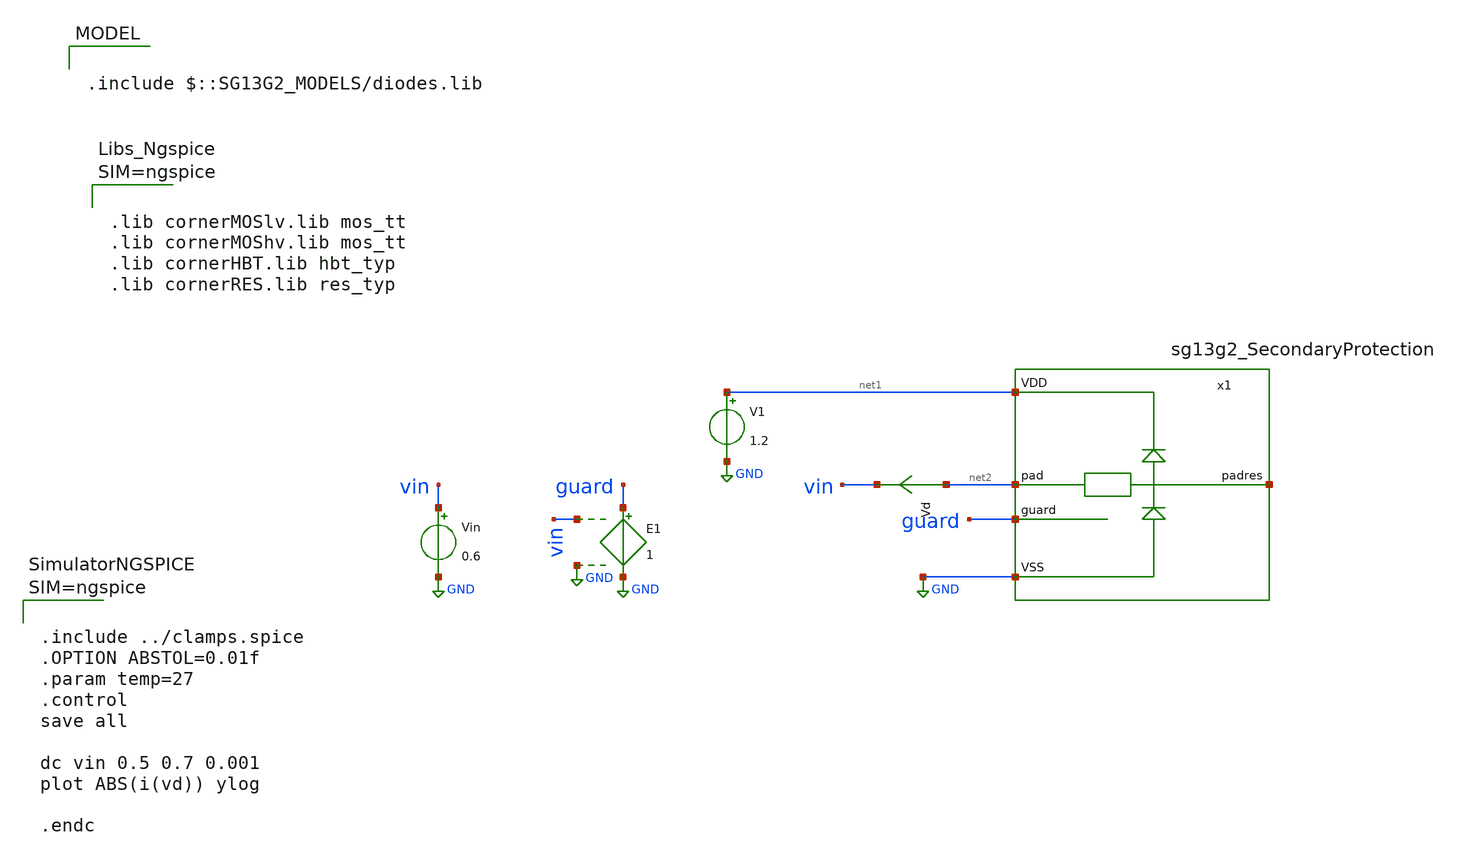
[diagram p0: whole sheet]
** sch_path: trident_test_structures/design_data/xschem/sg13g2_SecondaryProtection_tb.sch
**.subckt sg13g2_SecondaryProtection_tb
Vd net2 vin 0
.save i(vd)
Vin vin GND 0.6
V1 net1 GND 1.2
E1 guard GND vin GND 1
x1 net1 net2 net3 guard GND sg13g2_SecondaryProtection
**** begin user architecture code



.lib cornerMOSlv.lib mos_tt
.lib cornerMOShv.lib mos_tt
.lib cornerHBT.lib hbt_typ
.lib cornerRES.lib res_typ







.include ../clamps.spice
.OPTION ABSTOL=0.01f
.param temp=27
.control
save all

dc vin 0.5 0.7 0.001
plot ABS(i(vd)) ylog

.endc




.include $::SG13G2_MODELS/diodes.lib

**** end user architecture code
**.ends
.GLOBAL GND
.end
